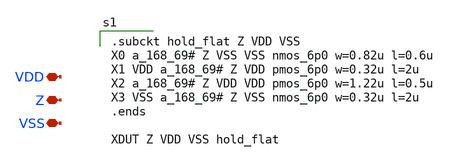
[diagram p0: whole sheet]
** sch_path: xschem/hold.sch
**.subckt hold VDD VSS Z
*.iopin VDD
*.iopin VSS
*.iopin Z
**** begin user architecture code

.subckt hold_flat Z VDD VSS
X0 a_168_69# Z VSS VSS nmos_6p0 w=0.82u l=0.6u
X1 VDD a_168_69# Z VDD pmos_6p0 w=0.32u l=2u
X2 a_168_69# Z VDD VDD pmos_6p0 w=1.22u l=0.5u
X3 VSS a_168_69# Z VSS nmos_6p0 w=0.32u l=2u
.ends

XDUT Z VDD VSS hold_flat



**** end user architecture code
**.ends
.end
